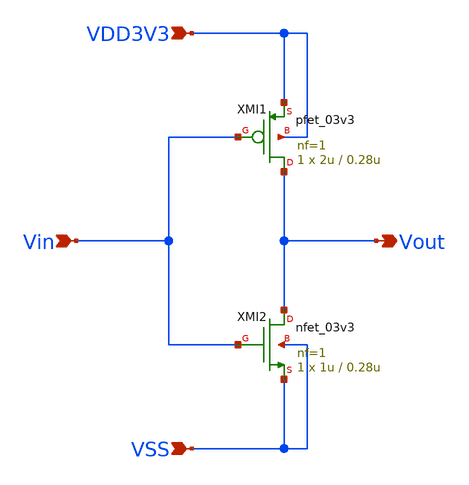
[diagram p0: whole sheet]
** sch_path: designs/libs/core_ina/ina_inv/ina_inv.sch
**.subckt ina_inv VDD3V3 VSS Vin Vout
*.ipin VDD3V3
*.ipin VSS
*.ipin Vin
*.opin Vout
XMI1 Vout Vin VDD3V3 VDD3V3 pfet_03v3 L=0.28u W=2u nf=1 ad='int((nf+1)/2) * W/nf * 0.18u' as='int((nf+2)/2) * W/nf * 0.18u'
+ pd='2*int((nf+1)/2) * (W/nf + 0.18u)' ps='2*int((nf+2)/2) * (W/nf + 0.18u)' nrd='0.18u / W' nrs='0.18u / W'
+ sa=0 sb=0 sd=0 m=1
XMI2 Vout Vin VSS VSS nfet_03v3 L=0.28u W=1u nf=1 ad='int((nf+1)/2) * W/nf * 0.18u' as='int((nf+2)/2) * W/nf * 0.18u'
+ pd='2*int((nf+1)/2) * (W/nf + 0.18u)' ps='2*int((nf+2)/2) * (W/nf + 0.18u)' nrd='0.18u / W' nrs='0.18u / W'
+ sa=0 sb=0 sd=0 m=1
**.ends
.end
